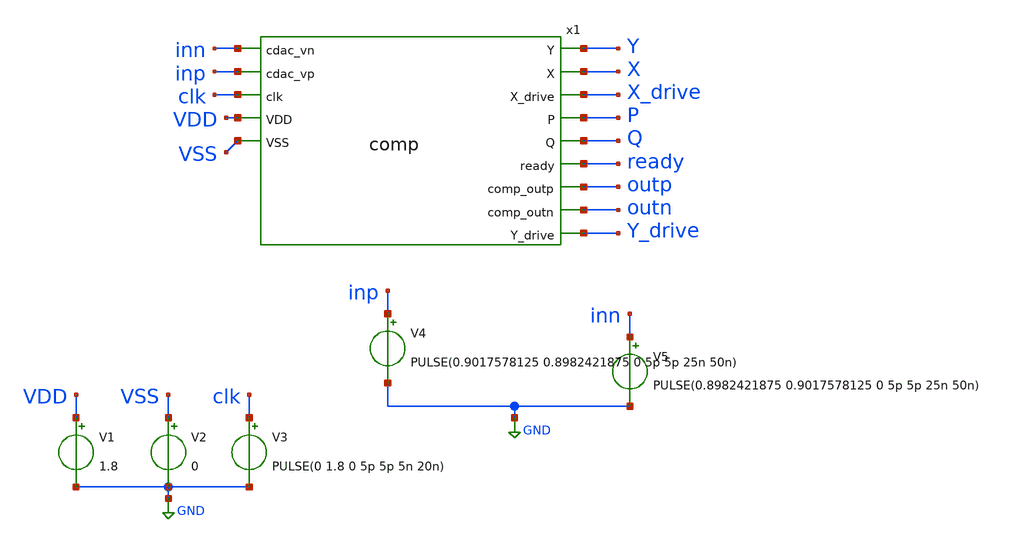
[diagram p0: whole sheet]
** sch_path: module/comparator/tb_comp.sch
**.subckt tb_comp
x1 Y X X_drive P Q ready inn outp outn inp clk Y_drive VDD VSS comp
V1 VDD GND 1.8
V2 VSS GND 0
V3 clk GND PULSE(0 1.8 0 5p 5p 5n 20n)
V4 inp GND PULSE(0.9017578125 0.8982421875 0 5p 5p 25n 50n)
V5 inn GND PULSE(0.8982421875 0.9017578125 0 5p 5p 25n 50n)
**** begin user architecture code



.lib /foss/pdks/sky130A/libs.tech/ngspice/sky130.lib.spice tt

.tran 1ns 100ns
.control
    run
    plot V(outp)+6 V(P)-2  V(X)+2  V(clk) V(inn) V(inp) V(Y)+2  V(outn)+6 V(Q)-2 V(ready)
+ V(X_drive)+4 V(Y_drive)+4
.endc
.save all



**** end user architecture code
**.ends

* expanding   symbol:  /foss/designs/goss_test/module/comparator/comp.sym # of pins=14
** sym_path: module/comparator/comp.sym
** sch_path: module/comparator/comp.sch
.subckt comp Y X X_drive P Q ready cdac_vn comp_outp comp_outn cdac_vp clk Y_drive VDD VSS
*.ipin cdac_vn
*.ipin cdac_vp
*.ipin VSS
*.ipin VDD
*.opin comp_outn
*.opin comp_outp
*.opin ready
*.ipin clk
*.opin X
*.opin Y
*.opin P
*.opin Q
*.opin X_drive
*.opin Y_drive
XM1 net1 clk VSS VSS sky130_fd_pr__nfet_01v8 L=0.15 W=4 nf=1 ad='int((nf+1)/2) * W/nf * 0.29' as='int((nf+2)/2) * W/nf * 0.29'
+ pd='2*int((nf+1)/2) * (W/nf + 0.29)' ps='2*int((nf+2)/2) * (W/nf + 0.29)' nrd='0.29 / W' nrs='0.29 / W'
+ sa=0 sb=0 sd=0 mult=1 m=1
XM4 Y X Q VSS sky130_fd_pr__nfet_01v8 L=0.15 W=4 nf=1 ad='int((nf+1)/2) * W/nf * 0.29' as='int((nf+2)/2) * W/nf * 0.29'
+ pd='2*int((nf+1)/2) * (W/nf + 0.29)' ps='2*int((nf+2)/2) * (W/nf + 0.29)' nrd='0.29 / W' nrs='0.29 / W'
+ sa=0 sb=0 sd=0 mult=1 m=1
XM5 X Y P VSS sky130_fd_pr__nfet_01v8 L=0.15 W=4 nf=1 ad='int((nf+1)/2) * W/nf * 0.29' as='int((nf+2)/2) * W/nf * 0.29'
+ pd='2*int((nf+1)/2) * (W/nf + 0.29)' ps='2*int((nf+2)/2) * (W/nf + 0.29)' nrd='0.29 / W' nrs='0.29 / W'
+ sa=0 sb=0 sd=0 mult=1 m=1
XM6 X Y VDD VDD sky130_fd_pr__pfet_01v8 L=0.15 W=2 nf=1 ad='int((nf+1)/2) * W/nf * 0.29' as='int((nf+2)/2) * W/nf * 0.29'
+ pd='2*int((nf+1)/2) * (W/nf + 0.29)' ps='2*int((nf+2)/2) * (W/nf + 0.29)' nrd='0.29 / W' nrs='0.29 / W'
+ sa=0 sb=0 sd=0 mult=1 m=1
XM7 Y X VDD VDD sky130_fd_pr__pfet_01v8 L=0.15 W=2 nf=1 ad='int((nf+1)/2) * W/nf * 0.29' as='int((nf+2)/2) * W/nf * 0.29'
+ pd='2*int((nf+1)/2) * (W/nf + 0.29)' ps='2*int((nf+2)/2) * (W/nf + 0.29)' nrd='0.29 / W' nrs='0.29 / W'
+ sa=0 sb=0 sd=0 mult=1 m=1
XM8 X clk VDD VDD sky130_fd_pr__pfet_01v8 L=0.15 W=2 nf=1 ad='int((nf+1)/2) * W/nf * 0.29' as='int((nf+2)/2) * W/nf * 0.29'
+ pd='2*int((nf+1)/2) * (W/nf + 0.29)' ps='2*int((nf+2)/2) * (W/nf + 0.29)' nrd='0.29 / W' nrs='0.29 / W'
+ sa=0 sb=0 sd=0 mult=1 m=1
XM9 P clk VDD VDD sky130_fd_pr__pfet_01v8 L=0.15 W=2 nf=1 ad='int((nf+1)/2) * W/nf * 0.29' as='int((nf+2)/2) * W/nf * 0.29'
+ pd='2*int((nf+1)/2) * (W/nf + 0.29)' ps='2*int((nf+2)/2) * (W/nf + 0.29)' nrd='0.29 / W' nrs='0.29 / W'
+ sa=0 sb=0 sd=0 mult=1 m=1
XM10 Y clk VDD VDD sky130_fd_pr__pfet_01v8 L=0.15 W=2 nf=1 ad='int((nf+1)/2) * W/nf * 0.29' as='int((nf+2)/2) * W/nf * 0.29'
+ pd='2*int((nf+1)/2) * (W/nf + 0.29)' ps='2*int((nf+2)/2) * (W/nf + 0.29)' nrd='0.29 / W' nrs='0.29 / W'
+ sa=0 sb=0 sd=0 mult=1 m=1
XM11 Q clk VDD VDD sky130_fd_pr__pfet_01v8 L=0.15 W=2 nf=1 ad='int((nf+1)/2) * W/nf * 0.29' as='int((nf+2)/2) * W/nf * 0.29'
+ pd='2*int((nf+1)/2) * (W/nf + 0.29)' ps='2*int((nf+2)/2) * (W/nf + 0.29)' nrd='0.29 / W' nrs='0.29 / W'
+ sa=0 sb=0 sd=0 mult=1 m=1
XM16 comp_outn comp_outp VDD VDD sky130_fd_pr__pfet_01v8 L=0.15 W=0.84 nf=1 ad='int((nf+1)/2) * W/nf * 0.29'
+ as='int((nf+2)/2) * W/nf * 0.29' pd='2*int((nf+1)/2) * (W/nf + 0.29)' ps='2*int((nf+2)/2) * (W/nf + 0.29)'
+ nrd='0.29 / W' nrs='0.29 / W' sa=0 sb=0 sd=0 mult=1 m=1
XM17 comp_outp comp_outn VDD VDD sky130_fd_pr__pfet_01v8 L=0.15 W=0.84 nf=1 ad='int((nf+1)/2) * W/nf * 0.29'
+ as='int((nf+2)/2) * W/nf * 0.29' pd='2*int((nf+1)/2) * (W/nf + 0.29)' ps='2*int((nf+2)/2) * (W/nf + 0.29)'
+ nrd='0.29 / W' nrs='0.29 / W' sa=0 sb=0 sd=0 mult=1 m=1
XM18 net3 Y_drive net2 VSS sky130_fd_pr__nfet_01v8 L=0.15 W=0.84 nf=1 ad='int((nf+1)/2) * W/nf * 0.29'
+ as='int((nf+2)/2) * W/nf * 0.29' pd='2*int((nf+1)/2) * (W/nf + 0.29)' ps='2*int((nf+2)/2) * (W/nf + 0.29)'
+ nrd='0.29 / W' nrs='0.29 / W' sa=0 sb=0 sd=0 mult=1 m=1
XM19 comp_outp Y_inv VSS VSS sky130_fd_pr__nfet_01v8 L=0.15 W=0.42 nf=1 ad='int((nf+1)/2) * W/nf * 0.29'
+ as='int((nf+2)/2) * W/nf * 0.29' pd='2*int((nf+1)/2) * (W/nf + 0.29)' ps='2*int((nf+2)/2) * (W/nf + 0.29)'
+ nrd='0.29 / W' nrs='0.29 / W' sa=0 sb=0 sd=0 mult=1 m=1
XM20 net3 Y_drive X_drive VDD sky130_fd_pr__pfet_01v8 L=0.15 W=0.84 nf=1 ad='int((nf+1)/2) * W/nf * 0.29'
+ as='int((nf+2)/2) * W/nf * 0.29' pd='2*int((nf+1)/2) * (W/nf + 0.29)' ps='2*int((nf+2)/2) * (W/nf + 0.29)'
+ nrd='0.29 / W' nrs='0.29 / W' sa=0 sb=0 sd=0 mult=1 m=1
XM21 net3 X_drive Y_drive VDD sky130_fd_pr__pfet_01v8 L=0.15 W=0.84 nf=1 ad='int((nf+1)/2) * W/nf * 0.29'
+ as='int((nf+2)/2) * W/nf * 0.29' pd='2*int((nf+1)/2) * (W/nf + 0.29)' ps='2*int((nf+2)/2) * (W/nf + 0.29)'
+ nrd='0.29 / W' nrs='0.29 / W' sa=0 sb=0 sd=0 mult=1 m=1
XM22 net2 X_drive VSS VSS sky130_fd_pr__nfet_01v8 L=0.15 W=0.84 nf=1 ad='int((nf+1)/2) * W/nf * 0.29'
+ as='int((nf+2)/2) * W/nf * 0.29' pd='2*int((nf+1)/2) * (W/nf + 0.29)' ps='2*int((nf+2)/2) * (W/nf + 0.29)'
+ nrd='0.29 / W' nrs='0.29 / W' sa=0 sb=0 sd=0 mult=1 m=1
XM23 comp_outn X_inv VSS VSS sky130_fd_pr__nfet_01v8 L=0.15 W=0.42 nf=1 ad='int((nf+1)/2) * W/nf * 0.29'
+ as='int((nf+2)/2) * W/nf * 0.29' pd='2*int((nf+1)/2) * (W/nf + 0.29)' ps='2*int((nf+2)/2) * (W/nf + 0.29)'
+ nrd='0.29 / W' nrs='0.29 / W' sa=0 sb=0 sd=0 mult=1 m=1
XM24 ready net3 VDD VDD sky130_fd_pr__pfet_01v8 L=0.15 W=0.84 nf=1 ad='int((nf+1)/2) * W/nf * 0.29' as='int((nf+2)/2) * W/nf * 0.29'
+ pd='2*int((nf+1)/2) * (W/nf + 0.29)' ps='2*int((nf+2)/2) * (W/nf + 0.29)' nrd='0.29 / W' nrs='0.29 / W'
+ sa=0 sb=0 sd=0 mult=1 m=1
XM25 ready net3 VSS VSS sky130_fd_pr__nfet_01v8 L=0.15 W=0.42 nf=1 ad='int((nf+1)/2) * W/nf * 0.29' as='int((nf+2)/2) * W/nf * 0.29'
+ pd='2*int((nf+1)/2) * (W/nf + 0.29)' ps='2*int((nf+2)/2) * (W/nf + 0.29)' nrd='0.29 / W' nrs='0.29 / W'
+ sa=0 sb=0 sd=0 mult=1 m=1
XM12 X_drive X_inv VDD VDD sky130_fd_pr__pfet_01v8 L=0.15 W='1.68 * 3 ' nf=3 ad='int((nf+1)/2) * W / nf * 0.29'
+ as='int((nf+2)/2) * W / nf * 0.29' pd='2*int((nf+1)/2) * (W / nf + 0.29)' ps='2*int((nf+2)/2) * (W / nf + 0.29)'
+ nrd='0.29 / W ' nrs='0.29 / W ' sa=0 sb=0 sd=0 mult=1 m=1
XM13 X_drive X_inv VSS VSS sky130_fd_pr__nfet_01v8 L=0.15 W='0.42 * 1 ' nf=1 ad='int((nf+1)/2) * W / nf * 0.29'
+ as='int((nf+2)/2) * W / nf * 0.29' pd='2*int((nf+1)/2) * (W / nf + 0.29)' ps='2*int((nf+2)/2) * (W / nf + 0.29)'
+ nrd='0.29 / W ' nrs='0.29 / W ' sa=0 sb=0 sd=0 mult=1 m=1
XM14 Y_drive Y_inv VDD VDD sky130_fd_pr__pfet_01v8 L=0.15 W='1.68 * 3 ' nf=3 ad='int((nf+1)/2) * W / nf * 0.29'
+ as='int((nf+2)/2) * W / nf * 0.29' pd='2*int((nf+1)/2) * (W / nf + 0.29)' ps='2*int((nf+2)/2) * (W / nf + 0.29)'
+ nrd='0.29 / W ' nrs='0.29 / W ' sa=0 sb=0 sd=0 mult=1 m=1
XM15 Y_drive Y_inv VSS VSS sky130_fd_pr__nfet_01v8 L=0.15 W='0.42 * 1 ' nf=1 ad='int((nf+1)/2) * W / nf * 0.29'
+ as='int((nf+2)/2) * W / nf * 0.29' pd='2*int((nf+1)/2) * (W / nf + 0.29)' ps='2*int((nf+2)/2) * (W / nf + 0.29)'
+ nrd='0.29 / W ' nrs='0.29 / W ' sa=0 sb=0 sd=0 mult=1 m=1
XM2 P cdac_vp net1 VSS sky130_fd_pr__nfet_01v8_lvt L=0.15 W='8 * 4 ' nf=4 ad='int((nf+1)/2) * W / nf * 0.29'
+ as='int((nf+2)/2) * W / nf * 0.29' pd='2*int((nf+1)/2) * (W / nf + 0.29)' ps='2*int((nf+2)/2) * (W / nf + 0.29)'
+ nrd='0.29 / W ' nrs='0.29 / W ' sa=0 sb=0 sd=0 mult=1 m=1
XM3 Q cdac_vn net1 VSS sky130_fd_pr__nfet_01v8_lvt L=0.15 W='8 * 4 ' nf=4 ad='int((nf+1)/2) * W / nf * 0.29'
+ as='int((nf+2)/2) * W / nf * 0.29' pd='2*int((nf+1)/2) * (W / nf + 0.29)' ps='2*int((nf+2)/2) * (W / nf + 0.29)'
+ nrd='0.29 / W ' nrs='0.29 / W ' sa=0 sb=0 sd=0 mult=1 m=1
XM26 X_inv X VDD VDD sky130_fd_pr__pfet_01v8 L=0.15 W=2 nf=1 ad='int((nf+1)/2) * W/nf * 0.29' as='int((nf+2)/2) * W/nf * 0.29'
+ pd='2*int((nf+1)/2) * (W/nf + 0.29)' ps='2*int((nf+2)/2) * (W/nf + 0.29)' nrd='0.29 / W' nrs='0.29 / W'
+ sa=0 sb=0 sd=0 mult=1 m=1
XM27 X_inv X VSS VSS sky130_fd_pr__nfet_01v8 L=0.15 W=4 nf=1 ad='int((nf+1)/2) * W/nf * 0.29' as='int((nf+2)/2) * W/nf * 0.29'
+ pd='2*int((nf+1)/2) * (W/nf + 0.29)' ps='2*int((nf+2)/2) * (W/nf + 0.29)' nrd='0.29 / W' nrs='0.29 / W'
+ sa=0 sb=0 sd=0 mult=1 m=1
XM28 Y_inv Y VDD VDD sky130_fd_pr__pfet_01v8 L=0.15 W=2 nf=1 ad='int((nf+1)/2) * W/nf * 0.29' as='int((nf+2)/2) * W/nf * 0.29'
+ pd='2*int((nf+1)/2) * (W/nf + 0.29)' ps='2*int((nf+2)/2) * (W/nf + 0.29)' nrd='0.29 / W' nrs='0.29 / W'
+ sa=0 sb=0 sd=0 mult=1 m=1
XM29 Y_inv Y VSS VSS sky130_fd_pr__nfet_01v8 L=0.15 W=4 nf=1 ad='int((nf+1)/2) * W/nf * 0.29' as='int((nf+2)/2) * W/nf * 0.29'
+ pd='2*int((nf+1)/2) * (W/nf + 0.29)' ps='2*int((nf+2)/2) * (W/nf + 0.29)' nrd='0.29 / W' nrs='0.29 / W'
+ sa=0 sb=0 sd=0 mult=1 m=1
.ends

.GLOBAL GND
.end
